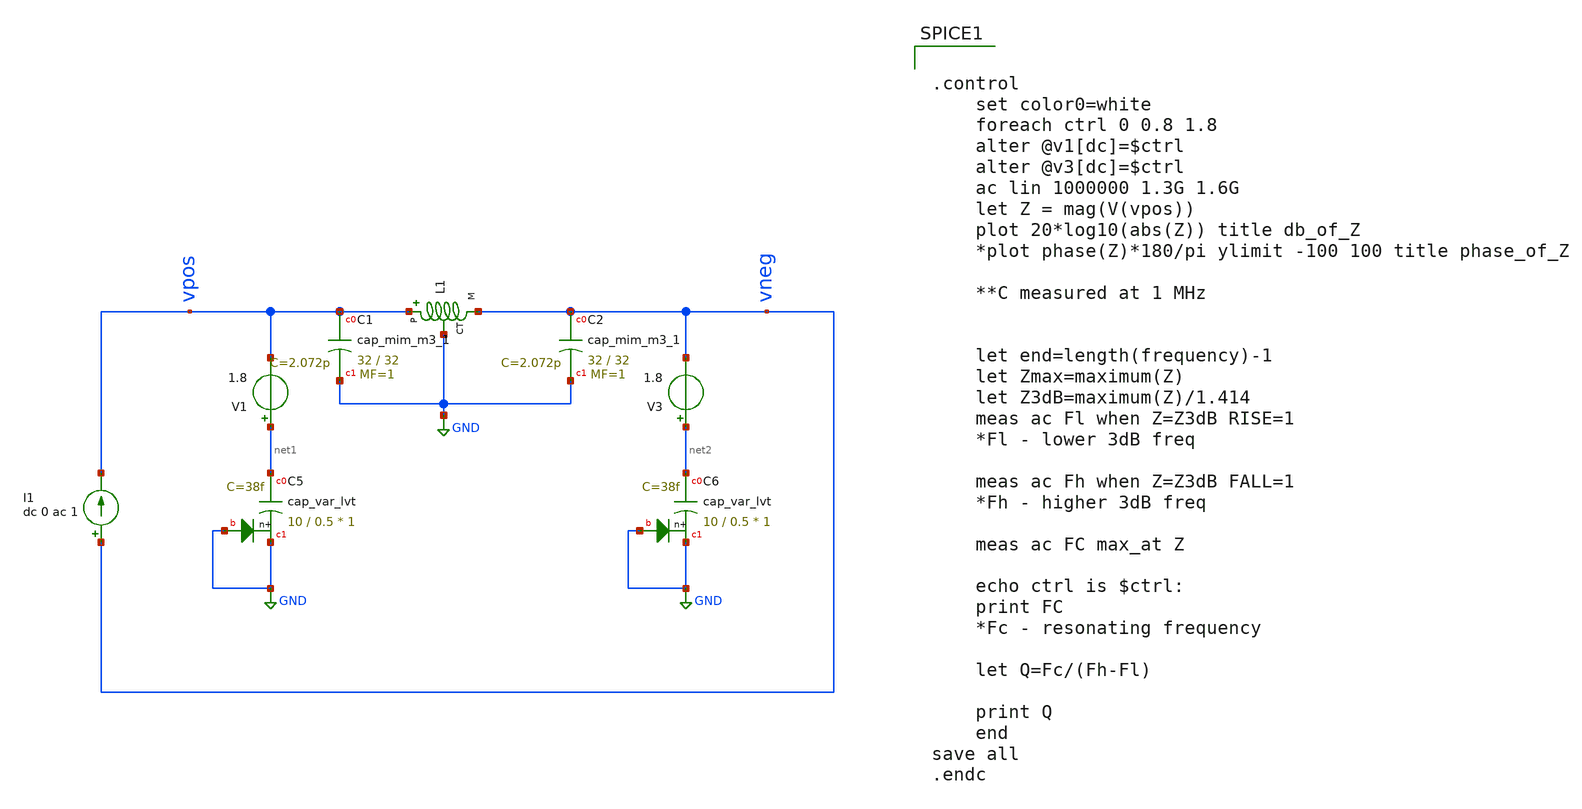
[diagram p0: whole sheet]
** sch_path: tank_meas/nonideal_tank.sch
**.subckt nonideal_tank
XC5 net1 GND GND sky130_fd_pr__cap_var_lvt W=10 L=0.5 VM=1 m=1
V1 net1 vpos 1.8
XC6 net2 GND GND sky130_fd_pr__cap_var_lvt W=10 L=0.5 VM=1 m=1
V3 net2 vneg 1.8
I1 vneg vpos dc 0 ac 1
XL1 vpos vneg GND GND sky130_fd_pr__ind_05_220
XC1 vpos GND sky130_fd_pr__cap_mim_m3_1 W=32 L=32 MF=1 m=1
XC2 vneg GND sky130_fd_pr__cap_mim_m3_1 W=32 L=32 MF=1 m=1
**** begin user architecture code


.option wnflag = 1
.lib /usr/local/share/pdk/sky130A/libs.tech/ngspice/sky130.lib.spice tt
.include /usr/local/share/pdk/sky130A/libs.ref/sky130_fd_pr/spice/sky130_fd_pr__ind_05_220.model.spice
.param mc_mm_switch=0




.control
	set color0=white
	foreach ctrl 0 0.8 1.8
	alter @v1[dc]=$ctrl
	alter @v3[dc]=$ctrl
	ac lin 1000000 1.3G 1.6G
	let Z = mag(V(vpos))
	plot 20*log10(abs(Z)) title db_of_Z
	*plot phase(Z)*180/pi ylimit -100 100 title phase_of_Z

	**C measured at 1 MHz


	let end=length(frequency)-1
	let Zmax=maximum(Z)
	let Z3dB=maximum(Z)/1.414
	meas ac Fl when Z=Z3dB RISE=1
	*Fl - lower 3dB freq

	meas ac Fh when Z=Z3dB FALL=1
	*Fh - higher 3dB freq

	meas ac FC max_at Z

	echo ctrl is $ctrl:
	print FC
	*Fc - resonating frequency

	let Q=Fc/(Fh-Fl)

	print Q
	end
save all
.endc


**** end user architecture code
**.ends
.GLOBAL GND
.end
